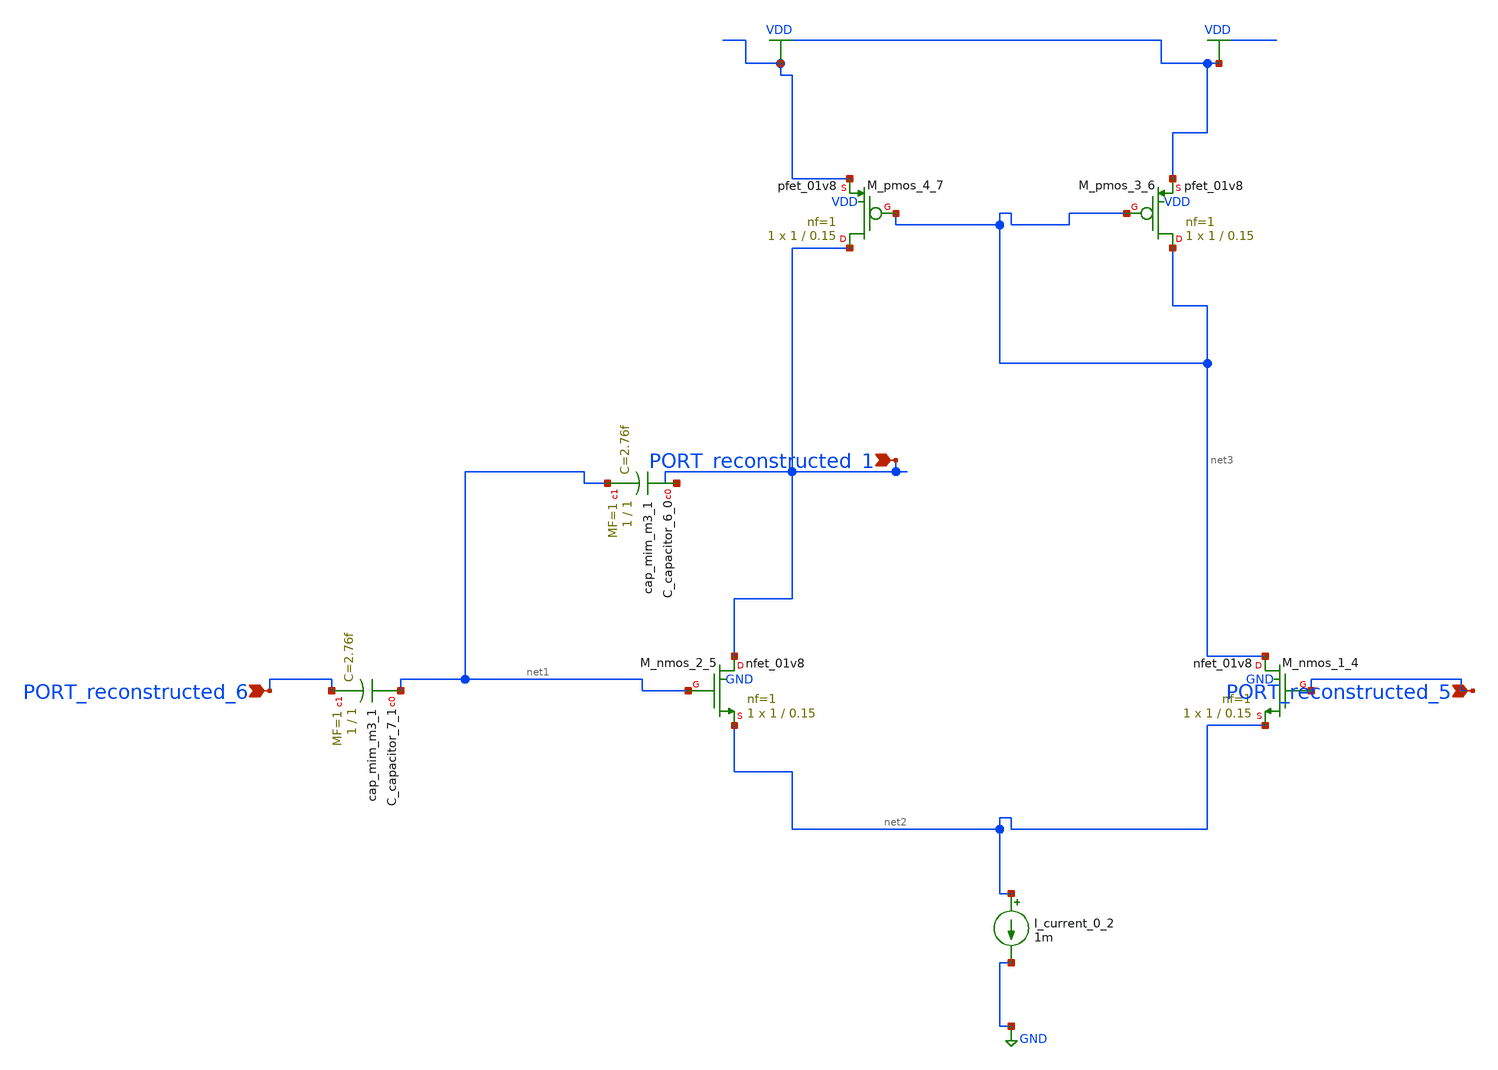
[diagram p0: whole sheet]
** sch_path: schematics/AMSNet/554.sch
**.subckt 554 PORT_reconstructed_5 PORT_reconstructed_1 PORT_reconstructed_6
*.ipin PORT_reconstructed_5
*.ipin PORT_reconstructed_1
*.ipin PORT_reconstructed_6
XC_capacitor_6_0 PORT_reconstructed_1 net1 sky130_fd_pr__cap_mim_m3_1 W=1 L=1 MF=1 m=1
XC_capacitor_7_1 net1 PORT_reconstructed_6 sky130_fd_pr__cap_mim_m3_1 W=1 L=1 MF=1 m=1
I_current_0_2 net2 GND 1m
XM_nmos_1_4 net3 PORT_reconstructed_5 net2 GND sky130_fd_pr__nfet_01v8 L=0.15 W=1 nf=1 ad='int((1 + 1)/2) * 1 / 1 * 0.29'
+ as='int((1 + 2)/2) * 1 / 1 * 0.29' pd='2*int((1 + 1)/2) * (1 / 1 + 0.29)' ps='2*int((1 + 2)/2) * (1 / 1 + 0.29)'
+ nrd='0.29 / 1 ' nrs='0.29 / 1 ' sa=0 sb=0 sd=0 mult=1 m=1
XM_nmos_2_5 PORT_reconstructed_1 net1 net2 GND sky130_fd_pr__nfet_01v8 L=0.15 W=1 nf=1 ad='int((1 + 1)/2) * 1 / 1 * 0.29'
+ as='int((1 + 2)/2) * 1 / 1 * 0.29' pd='2*int((1 + 1)/2) * (1 / 1 + 0.29)' ps='2*int((1 + 2)/2) * (1 / 1 + 0.29)'
+ nrd='0.29 / 1 ' nrs='0.29 / 1 ' sa=0 sb=0 sd=0 mult=1 m=1
XM_pmos_3_6 net3 net3 VDD VDD sky130_fd_pr__pfet_01v8 L=0.15 W=1 nf=1 ad='int((1 + 1)/2) * 1 / 1 * 0.29'
+ as='int((1 + 2)/2) * 1 / 1 * 0.29' pd='2*int((1 + 1)/2) * (1 / 1 + 0.29)' ps='2*int((1 + 2)/2) * (1 / 1 + 0.29)'
+ nrd='0.29 / 1 ' nrs='0.29 / 1 ' sa=0 sb=0 sd=0 mult=1 m=1
XM_pmos_4_7 PORT_reconstructed_1 net3 VDD VDD sky130_fd_pr__pfet_01v8 L=0.15 W=1 nf=1 ad='int((1 + 1)/2) * 1 / 1 * 0.29'
+ as='int((1 + 2)/2) * 1 / 1 * 0.29' pd='2*int((1 + 1)/2) * (1 / 1 + 0.29)' ps='2*int((1 + 2)/2) * (1 / 1 + 0.29)'
+ nrd='0.29 / 1 ' nrs='0.29 / 1 ' sa=0 sb=0 sd=0 mult=1 m=1
**.ends
.GLOBAL GND
.GLOBAL VDD
.end
